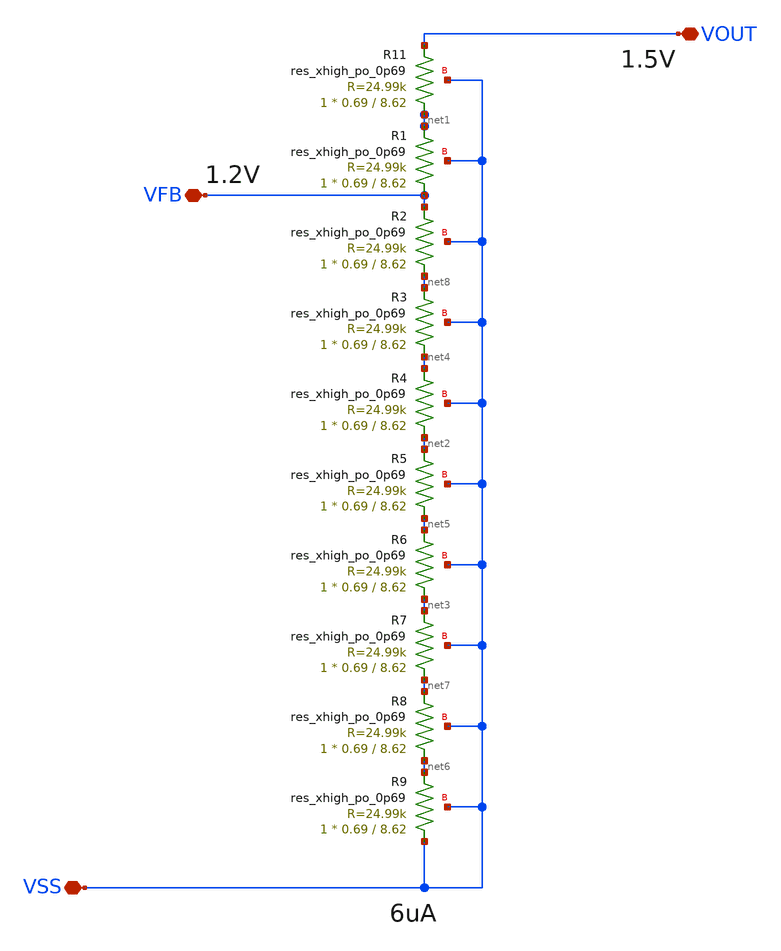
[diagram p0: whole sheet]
** sch_path: RES_FB/RES_FB.sch
**.subckt RES_FB VOUT VFB VSS
*.iopin VOUT
*.iopin VFB
*.iopin VSS
XR11 net1 VOUT VSS sky130_fd_pr__res_xhigh_po_0p69 L=8.62 mult=1 m=1
XR1 VFB net1 VSS sky130_fd_pr__res_xhigh_po_0p69 L=8.62 mult=1 m=1
XR2 net8 VFB VSS sky130_fd_pr__res_xhigh_po_0p69 L=8.62 mult=1 m=1
XR3 net4 net8 VSS sky130_fd_pr__res_xhigh_po_0p69 L=8.62 mult=1 m=1
XR4 net2 net4 VSS sky130_fd_pr__res_xhigh_po_0p69 L=8.62 mult=1 m=1
XR5 net5 net2 VSS sky130_fd_pr__res_xhigh_po_0p69 L=8.62 mult=1 m=1
XR6 net3 net5 VSS sky130_fd_pr__res_xhigh_po_0p69 L=8.62 mult=1 m=1
XR7 net7 net3 VSS sky130_fd_pr__res_xhigh_po_0p69 L=8.62 mult=1 m=1
XR8 net6 net7 VSS sky130_fd_pr__res_xhigh_po_0p69 L=8.62 mult=1 m=1
XR9 VSS net6 VSS sky130_fd_pr__res_xhigh_po_0p69 L=8.62 mult=1 m=1
**.ends
.end
